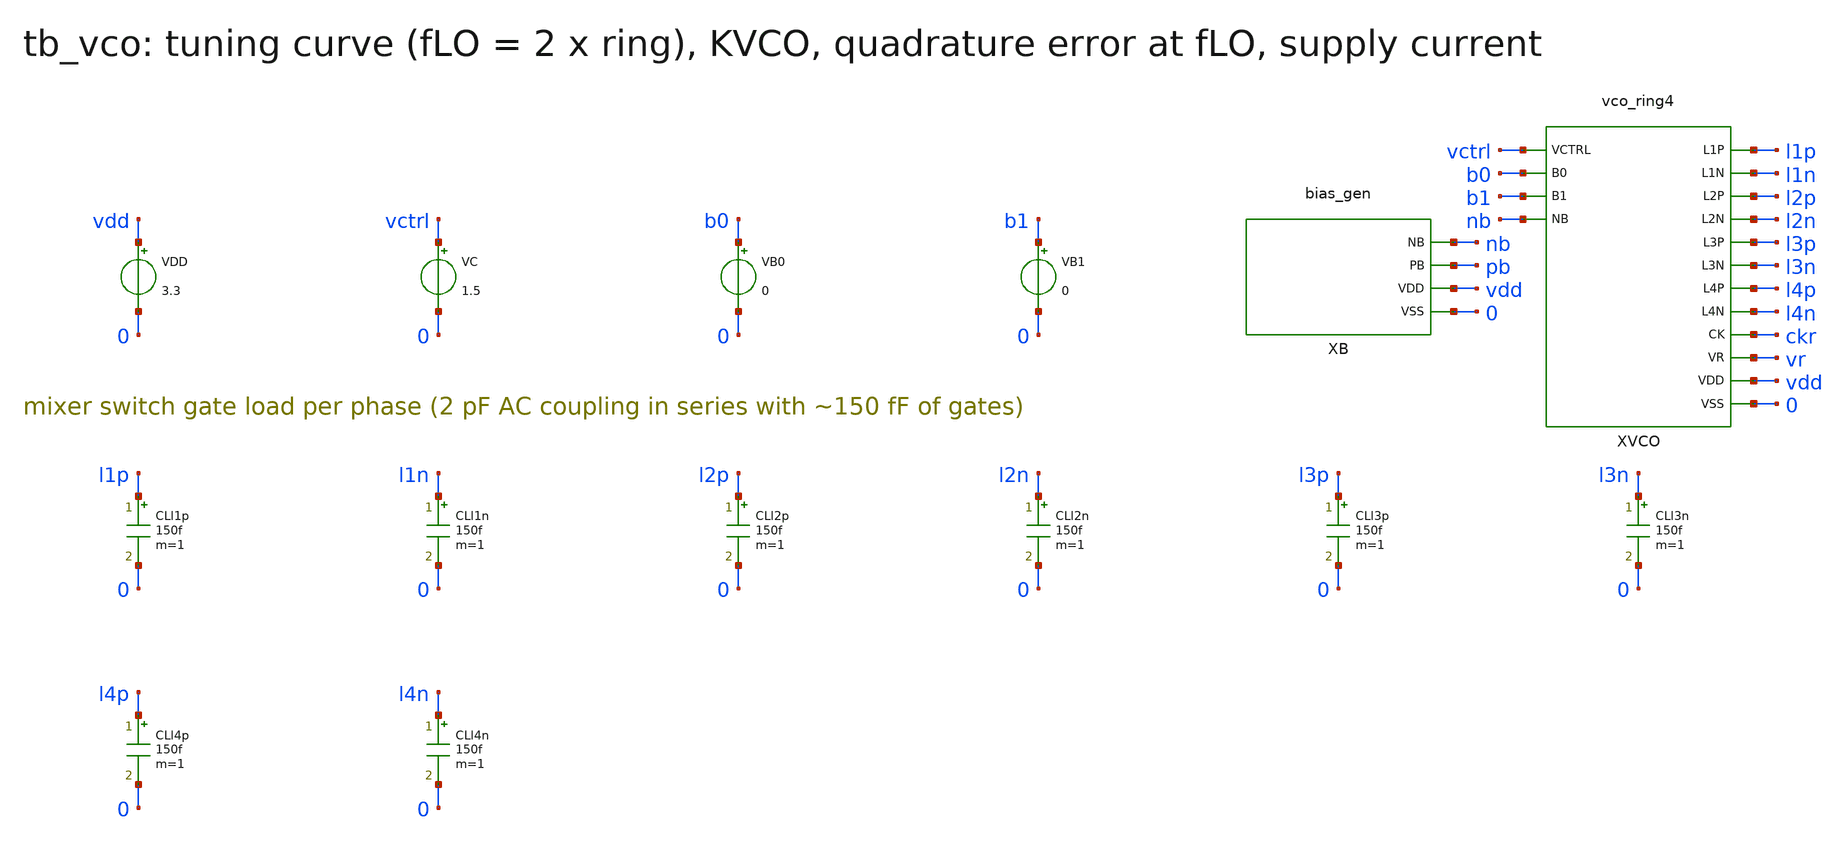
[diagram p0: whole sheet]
** sch_path: v1_claude/xschem/tb_vco.sch
**.subckt tb_vco
VDD vdd 0 3.3
VC vctrl 0 1.5
VB0 b0 0 0
VB1 b1 0 0
XB nb pb vdd 0 bias_gen
XVCO vctrl b0 b1 nb l1p l1n l2p l2n l3p l3n l4p l4n ckr vr vdd 0 vco_ring4
CLl1p l1p 0 150f m=1
CLl1n l1n 0 150f m=1
CLl2p l2p 0 150f m=1
CLl2n l2n 0 150f m=1
CLl3p l3p 0 150f m=1
CLl3n l3n 0 150f m=1
CLl4p l4p 0 150f m=1
CLl4n l4n 0 150f m=1
**** begin user architecture code
 .include $::180MCU_MODELS/design.ngspice
.lib $::180MCU_MODELS/sm141064.ngspice typical
.lib $::180MCU_MODELS/sm141064.ngspice res_typical
.lib $::180MCU_MODELS/sm141064.ngspice mimcap_typical

.option method=gear reltol=1e-4
.ic v(xvco.xcore.p4)=0 v(xvco.xcore.n4)=2
.control
set num_threads=1
let vlist = vector(9)*0.25+0.8
let k = 0
while k < 9
 let vv = vlist[k]
 alter VC dc = vv
 tran 2p 70n uic
 meas tran ta when v(l1p)=v(l1n) rise=1 td=55n
 meas tran tb when v(l1p)=v(l1n) rise=5 td=55n
 meas tran tq when v(l2p)=v(l2n) rise=1 td=55n
 meas tran ivdd avg i(VDD) from=55n to=70n
 meas tran vravg avg v(vr) from=55n to=70n
 let f = 8/(tb-ta)
 let qerr = ((tq-ta)*f/2 - floor((tq-ta)*f/2))*720 - 90
 echo RES vc=$&vv f=$&f qerr=$&qerr ivdd=$&ivdd vr=$&vravg
 let k = k + 1
end
.endc

**** end user architecture code
**.ends
.end
